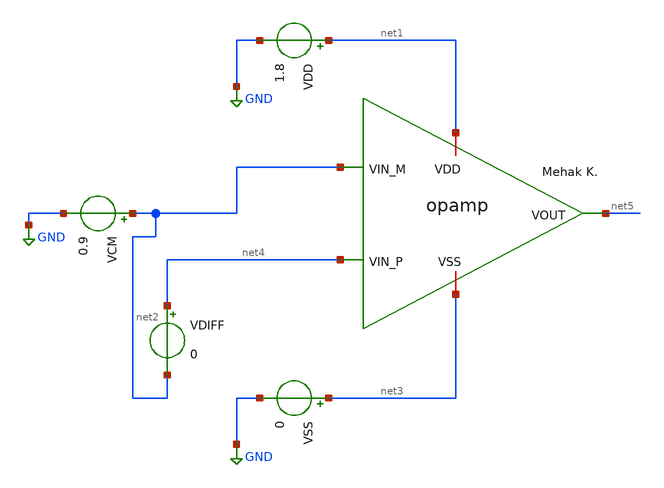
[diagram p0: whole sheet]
** sch_path: analog/build/schematic/tb_dc_analysis.sch
**.subckt tb_dc_analysis
VDD net1 GND 1.8
VSS net3 GND 0
VCM net2 GND 0.9
VDIFF net4 net2 0
x1 net1 net5 net2 net4 net3 opamp_two_stage
**** begin user architecture code


.lib /home/mehak/.volare/volare/sky130/versions/fa87f8f4bbcc7255b6f0c0fb506960f531ae2392/sky130A/libs.tech/ngspice/sky130.lib.spice tt
.dc VDIFF -0.01 0.01 0.0001
.save all


**** end user architecture code
**.ends
.GLOBAL GND
.end
